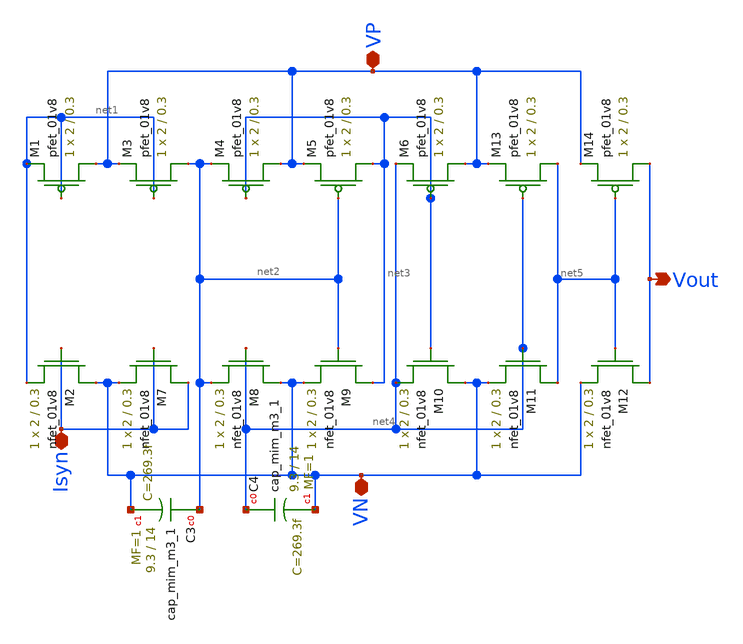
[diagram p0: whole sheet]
** sch_path: schematic/besrour_neuron_cm_lds.sch
**.subckt besrour_neuron_cm_lds VP VN Isyn Vout
*.iopin VP
*.iopin VN
*.iopin Isyn
*.opin Vout
XM2 VN Isyn net1 GND sky130_fd_pr__nfet_01v8 L=0.3 W=2 nf=1 ad='int((nf+1)/2) * W/nf * 0.29' as='int((nf+2)/2) * W/nf * 0.29'
+ pd='2*int((nf+1)/2) * (W/nf + 0.29)' ps='2*int((nf+2)/2) * (W/nf + 0.29)' nrd='0.29 / W' nrs='0.29 / W'
+ sa=0 sb=0 sd=0 mult=1 m=1
XM3 net2 net1 VP VDD sky130_fd_pr__pfet_01v8 L=0.3 W=2 nf=1 ad='int((nf+1)/2) * W/nf * 0.29' as='int((nf+2)/2) * W/nf * 0.29'
+ pd='2*int((nf+1)/2) * (W/nf + 0.29)' ps='2*int((nf+2)/2) * (W/nf + 0.29)' nrd='0.29 / W' nrs='0.29 / W'
+ sa=0 sb=0 sd=0 mult=1 m=1
XC3 net2 VN sky130_fd_pr__cap_mim_m3_1 W=9.3 L=14 MF=1 m=1
XC4 net4 VN sky130_fd_pr__cap_mim_m3_1 W=9.3 L=14 MF=1 m=1
XM4 VP net3 net2 VDD sky130_fd_pr__pfet_01v8 L=0.3 W=2 nf=1 ad='int((nf+1)/2) * W/nf * 0.29' as='int((nf+2)/2) * W/nf * 0.29'
+ pd='2*int((nf+1)/2) * (W/nf + 0.29)' ps='2*int((nf+2)/2) * (W/nf + 0.29)' nrd='0.29 / W' nrs='0.29 / W'
+ sa=0 sb=0 sd=0 mult=1 m=1
XM5 net3 net2 VP VDD sky130_fd_pr__pfet_01v8 L=0.3 W=2 nf=1 ad='int((nf+1)/2) * W/nf * 0.29' as='int((nf+2)/2) * W/nf * 0.29'
+ pd='2*int((nf+1)/2) * (W/nf + 0.29)' ps='2*int((nf+2)/2) * (W/nf + 0.29)' nrd='0.29 / W' nrs='0.29 / W'
+ sa=0 sb=0 sd=0 mult=1 m=1
XM6 VP net3 net4 VDD sky130_fd_pr__pfet_01v8 L=0.3 W=2 nf=1 ad='int((nf+1)/2) * W/nf * 0.29' as='int((nf+2)/2) * W/nf * 0.29'
+ pd='2*int((nf+1)/2) * (W/nf + 0.29)' ps='2*int((nf+2)/2) * (W/nf + 0.29)' nrd='0.29 / W' nrs='0.29 / W'
+ sa=0 sb=0 sd=0 mult=1 m=1
XM13 net5 net4 VP VDD sky130_fd_pr__pfet_01v8 L=0.3 W=2 nf=1 ad='int((nf+1)/2) * W/nf * 0.29' as='int((nf+2)/2) * W/nf * 0.29'
+ pd='2*int((nf+1)/2) * (W/nf + 0.29)' ps='2*int((nf+2)/2) * (W/nf + 0.29)' nrd='0.29 / W' nrs='0.29 / W'
+ sa=0 sb=0 sd=0 mult=1 m=1
XM14 Vout net5 VP VDD sky130_fd_pr__pfet_01v8 L=0.3 W=2 nf=1 ad='int((nf+1)/2) * W/nf * 0.29' as='int((nf+2)/2) * W/nf * 0.29'
+ pd='2*int((nf+1)/2) * (W/nf + 0.29)' ps='2*int((nf+2)/2) * (W/nf + 0.29)' nrd='0.29 / W' nrs='0.29 / W'
+ sa=0 sb=0 sd=0 mult=1 m=1
XM1 VP net1 net1 VDD sky130_fd_pr__pfet_01v8 L=0.3 W=2 nf=1 ad='int((nf+1)/2) * W/nf * 0.29' as='int((nf+2)/2) * W/nf * 0.29'
+ pd='2*int((nf+1)/2) * (W/nf + 0.29)' ps='2*int((nf+2)/2) * (W/nf + 0.29)' nrd='0.29 / W' nrs='0.29 / W'
+ sa=0 sb=0 sd=0 mult=1 m=1
XM7 Isyn Isyn VN GND sky130_fd_pr__nfet_01v8 L=0.3 W=2 nf=1 ad='int((nf+1)/2) * W/nf * 0.29' as='int((nf+2)/2) * W/nf * 0.29'
+ pd='2*int((nf+1)/2) * (W/nf + 0.29)' ps='2*int((nf+2)/2) * (W/nf + 0.29)' nrd='0.29 / W' nrs='0.29 / W'
+ sa=0 sb=0 sd=0 mult=1 m=1
XM8 VN net4 net2 GND sky130_fd_pr__nfet_01v8 L=0.3 W=2 nf=1 ad='int((nf+1)/2) * W/nf * 0.29' as='int((nf+2)/2) * W/nf * 0.29'
+ pd='2*int((nf+1)/2) * (W/nf + 0.29)' ps='2*int((nf+2)/2) * (W/nf + 0.29)' nrd='0.29 / W' nrs='0.29 / W'
+ sa=0 sb=0 sd=0 mult=1 m=1
XM9 net3 net2 VN GND sky130_fd_pr__nfet_01v8 L=0.3 W=2 nf=1 ad='int((nf+1)/2) * W/nf * 0.29' as='int((nf+2)/2) * W/nf * 0.29'
+ pd='2*int((nf+1)/2) * (W/nf + 0.29)' ps='2*int((nf+2)/2) * (W/nf + 0.29)' nrd='0.29 / W' nrs='0.29 / W'
+ sa=0 sb=0 sd=0 mult=1 m=1
XM10 VN net3 net4 GND sky130_fd_pr__nfet_01v8 L=0.3 W=2 nf=1 ad='int((nf+1)/2) * W/nf * 0.29' as='int((nf+2)/2) * W/nf * 0.29'
+ pd='2*int((nf+1)/2) * (W/nf + 0.29)' ps='2*int((nf+2)/2) * (W/nf + 0.29)' nrd='0.29 / W' nrs='0.29 / W'
+ sa=0 sb=0 sd=0 mult=1 m=1
XM11 net5 net4 VN GND sky130_fd_pr__nfet_01v8 L=0.3 W=2 nf=1 ad='int((nf+1)/2) * W/nf * 0.29' as='int((nf+2)/2) * W/nf * 0.29'
+ pd='2*int((nf+1)/2) * (W/nf + 0.29)' ps='2*int((nf+2)/2) * (W/nf + 0.29)' nrd='0.29 / W' nrs='0.29 / W'
+ sa=0 sb=0 sd=0 mult=1 m=1
XM12 Vout net5 VN GND sky130_fd_pr__nfet_01v8 L=0.3 W=2 nf=1 ad='int((nf+1)/2) * W/nf * 0.29' as='int((nf+2)/2) * W/nf * 0.29'
+ pd='2*int((nf+1)/2) * (W/nf + 0.29)' ps='2*int((nf+2)/2) * (W/nf + 0.29)' nrd='0.29 / W' nrs='0.29 / W'
+ sa=0 sb=0 sd=0 mult=1 m=1
**.ends
.end
